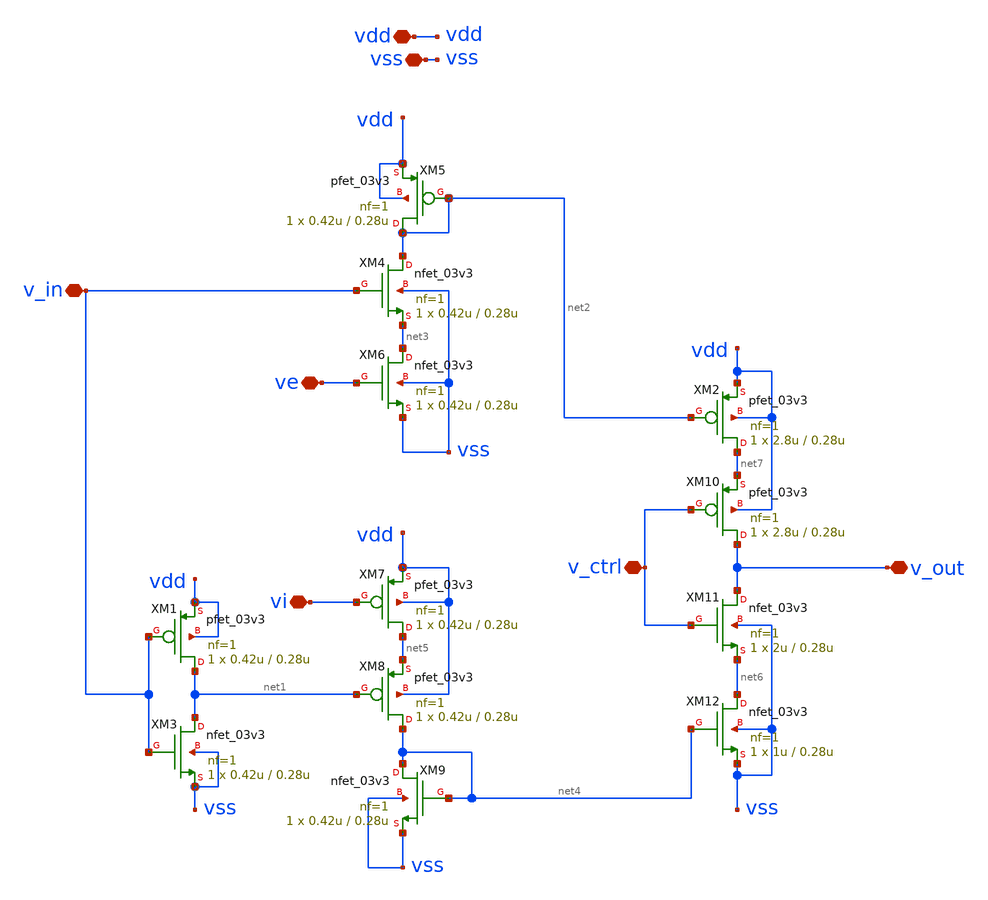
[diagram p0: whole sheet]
** sch_path: designs/libs/core_synapse/synapse.sch
**.subckt synapse v_out v_ctrl ve vi v_in vdd vss
*.iopin v_out
*.iopin v_ctrl
*.iopin ve
*.iopin vi
*.iopin v_in
*.iopin vdd
*.iopin vss
XM5 net2 net2 vdd vdd pfet_03v3 L=0.28u W=0.42u nf=1 ad='int((nf+1)/2) * W/nf * 0.18u' as='int((nf+2)/2) * W/nf * 0.18u'
+ pd='2*int((nf+1)/2) * (W/nf + 0.18u)' ps='2*int((nf+2)/2) * (W/nf + 0.18u)' nrd='0.18u / W' nrs='0.18u / W'
+ sa=0 sb=0 sd=0 m=1
XM1 net1 v_in vdd vdd pfet_03v3 L=0.28u W=0.42u nf=1 ad='int((nf+1)/2) * W/nf * 0.18u' as='int((nf+2)/2) * W/nf * 0.18u'
+ pd='2*int((nf+1)/2) * (W/nf + 0.18u)' ps='2*int((nf+2)/2) * (W/nf + 0.18u)' nrd='0.18u / W' nrs='0.18u / W'
+ sa=0 sb=0 sd=0 m=1
XM3 net1 v_in vss vss nfet_03v3 L=0.28u W=0.42u nf=1 ad='int((nf+1)/2) * W/nf * 0.18u' as='int((nf+2)/2) * W/nf * 0.18u'
+ pd='2*int((nf+1)/2) * (W/nf + 0.18u)' ps='2*int((nf+2)/2) * (W/nf + 0.18u)' nrd='0.18u / W' nrs='0.18u / W'
+ sa=0 sb=0 sd=0 m=1
XM4 net2 v_in net3 vss nfet_03v3 L=0.28u W=0.42u nf=1 ad='int((nf+1)/2) * W/nf * 0.18u' as='int((nf+2)/2) * W/nf * 0.18u'
+ pd='2*int((nf+1)/2) * (W/nf + 0.18u)' ps='2*int((nf+2)/2) * (W/nf + 0.18u)' nrd='0.18u / W' nrs='0.18u / W'
+ sa=0 sb=0 sd=0 m=1
XM6 net3 ve vss vss nfet_03v3 L=0.28u W=0.42u nf=1 ad='int((nf+1)/2) * W/nf * 0.18u' as='int((nf+2)/2) * W/nf * 0.18u'
+ pd='2*int((nf+1)/2) * (W/nf + 0.18u)' ps='2*int((nf+2)/2) * (W/nf + 0.18u)' nrd='0.18u / W' nrs='0.18u / W'
+ sa=0 sb=0 sd=0 m=1
XM7 net5 vi vdd vdd pfet_03v3 L=0.28u W=0.42u nf=1 ad='int((nf+1)/2) * W/nf * 0.18u' as='int((nf+2)/2) * W/nf * 0.18u'
+ pd='2*int((nf+1)/2) * (W/nf + 0.18u)' ps='2*int((nf+2)/2) * (W/nf + 0.18u)' nrd='0.18u / W' nrs='0.18u / W'
+ sa=0 sb=0 sd=0 m=1
XM8 net4 net1 net5 vdd pfet_03v3 L=0.28u W=0.42u nf=1 ad='int((nf+1)/2) * W/nf * 0.18u' as='int((nf+2)/2) * W/nf * 0.18u'
+ pd='2*int((nf+1)/2) * (W/nf + 0.18u)' ps='2*int((nf+2)/2) * (W/nf + 0.18u)' nrd='0.18u / W' nrs='0.18u / W'
+ sa=0 sb=0 sd=0 m=1
XM9 net4 net4 vss vss nfet_03v3 L=0.28u W=0.42u nf=1 ad='int((nf+1)/2) * W/nf * 0.18u' as='int((nf+2)/2) * W/nf * 0.18u'
+ pd='2*int((nf+1)/2) * (W/nf + 0.18u)' ps='2*int((nf+2)/2) * (W/nf + 0.18u)' nrd='0.18u / W' nrs='0.18u / W'
+ sa=0 sb=0 sd=0 m=1
XM2 net7 net2 vdd vdd pfet_03v3 L=0.28u W=2.8u nf=1 ad='int((nf+1)/2) * W/nf * 0.18u' as='int((nf+2)/2) * W/nf * 0.18u'
+ pd='2*int((nf+1)/2) * (W/nf + 0.18u)' ps='2*int((nf+2)/2) * (W/nf + 0.18u)' nrd='0.18u / W' nrs='0.18u / W'
+ sa=0 sb=0 sd=0 m=1
XM10 v_out v_ctrl net7 vdd pfet_03v3 L=0.28u W=2.8u nf=1 ad='int((nf+1)/2) * W/nf * 0.18u' as='int((nf+2)/2) * W/nf * 0.18u'
+ pd='2*int((nf+1)/2) * (W/nf + 0.18u)' ps='2*int((nf+2)/2) * (W/nf + 0.18u)' nrd='0.18u / W' nrs='0.18u / W'
+ sa=0 sb=0 sd=0 m=1
XM11 v_out v_ctrl net6 vss nfet_03v3 L=0.28u W=2u nf=1 ad='int((nf+1)/2) * W/nf * 0.18u' as='int((nf+2)/2) * W/nf * 0.18u'
+ pd='2*int((nf+1)/2) * (W/nf + 0.18u)' ps='2*int((nf+2)/2) * (W/nf + 0.18u)' nrd='0.18u / W' nrs='0.18u / W'
+ sa=0 sb=0 sd=0 m=1
XM12 net6 net4 vss vss nfet_03v3 L=0.28u W=1u nf=1 ad='int((nf+1)/2) * W/nf * 0.18u' as='int((nf+2)/2) * W/nf * 0.18u'
+ pd='2*int((nf+1)/2) * (W/nf + 0.18u)' ps='2*int((nf+2)/2) * (W/nf + 0.18u)' nrd='0.18u / W' nrs='0.18u / W'
+ sa=0 sb=0 sd=0 m=1
**.ends
.end
